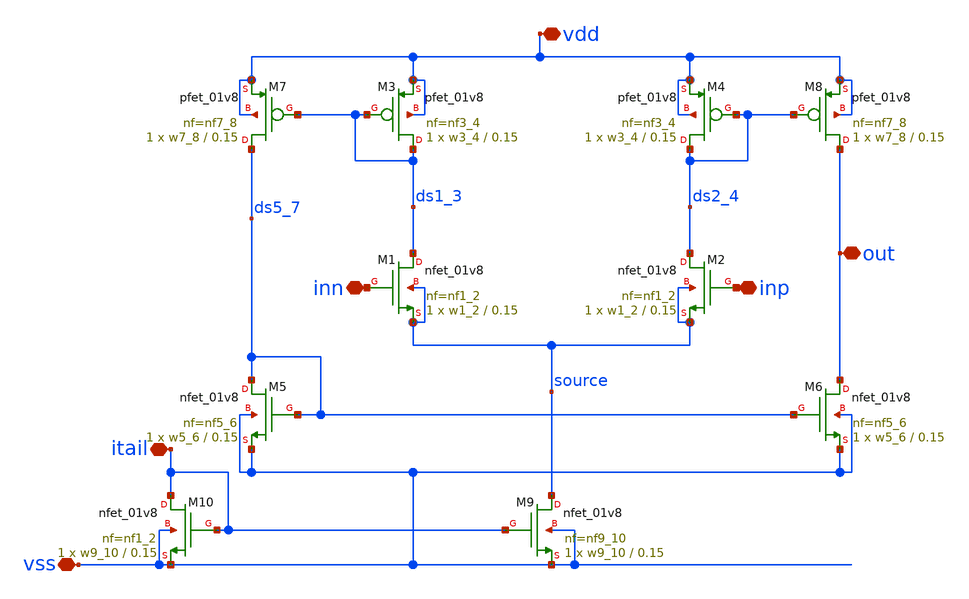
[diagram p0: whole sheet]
** sch_path: ISSCC25/submitted_notebooks/current_mirror_ota_optimization/characterization/sky130/schematics/cm_ota.sch
**.subckt cm_ota inn inp out vss vdd itail
*.iopin inn
*.iopin inp
*.iopin out
*.iopin vss
*.iopin vdd
*.iopin itail
XM1 ds1_3 inn source source sky130_fd_pr__nfet_01v8 L=0.15 W=w1_2 nf=nf1_2 ad='int((nf+1)/2) * W/nf * 0.29'
+ as='int((nf+2)/2) * W/nf * 0.29' pd='2*int((nf+1)/2) * (W/nf + 0.29)' ps='2*int((nf+2)/2) * (W/nf + 0.29)'
+ nrd='0.29 / W' nrs='0.29 / W' sa=0 sb=0 sd=0 mult=1 m=1
xM3 ds1_3 ds1_3 vdd vdd sky130_fd_pr__pfet_01v8 L=0.15 W=w3_4 nf=nf3_4 ad='int((nf+1)/2) * W/nf * 0.29'
+ as='int((nf+2)/2) * W/nf * 0.29' pd='2*int((nf+1)/2) * (W/nf + 0.29)' ps='2*int((nf+2)/2) * (W/nf + 0.29)'
+ nrd='0.29 / W' nrs='0.29 / W' sa=0 sb=0 sd=0 mult=1 m=1
XM2 ds2_4 inp source source sky130_fd_pr__nfet_01v8 L=0.15 W=w1_2 nf=nf1_2 ad='int((nf+1)/2) * W/nf * 0.29'
+ as='int((nf+2)/2) * W/nf * 0.29' pd='2*int((nf+1)/2) * (W/nf + 0.29)' ps='2*int((nf+2)/2) * (W/nf + 0.29)'
+ nrd='0.29 / W' nrs='0.29 / W' sa=0 sb=0 sd=0 mult=1 m=1
xM4 ds2_4 ds2_4 vdd vdd sky130_fd_pr__pfet_01v8 L=0.15 W=w3_4 nf=nf3_4 ad='int((nf+1)/2) * W/nf * 0.29'
+ as='int((nf+2)/2) * W/nf * 0.29' pd='2*int((nf+1)/2) * (W/nf + 0.29)' ps='2*int((nf+2)/2) * (W/nf + 0.29)'
+ nrd='0.29 / W' nrs='0.29 / W' sa=0 sb=0 sd=0 mult=1 m=1
xM7 ds5_7 ds1_3 vdd vdd sky130_fd_pr__pfet_01v8 L=0.15 W=w7_8 nf=nf7_8 ad='int((nf+1)/2) * W/nf * 0.29'
+ as='int((nf+2)/2) * W/nf * 0.29' pd='2*int((nf+1)/2) * (W/nf + 0.29)' ps='2*int((nf+2)/2) * (W/nf + 0.29)'
+ nrd='0.29 / W' nrs='0.29 / W' sa=0 sb=0 sd=0 mult=1 m=1
XM5 ds5_7 ds5_7 vss vss sky130_fd_pr__nfet_01v8 L=0.15 W=w5_6 nf=nf5_6 ad='int((nf+1)/2) * W/nf * 0.29'
+ as='int((nf+2)/2) * W/nf * 0.29' pd='2*int((nf+1)/2) * (W/nf + 0.29)' ps='2*int((nf+2)/2) * (W/nf + 0.29)'
+ nrd='0.29 / W' nrs='0.29 / W' sa=0 sb=0 sd=0 mult=1 m=1
XM6 out ds5_7 vss vss sky130_fd_pr__nfet_01v8 L=0.15 W=w5_6 nf=nf5_6 ad='int((nf+1)/2) * W/nf * 0.29'
+ as='int((nf+2)/2) * W/nf * 0.29' pd='2*int((nf+1)/2) * (W/nf + 0.29)' ps='2*int((nf+2)/2) * (W/nf + 0.29)'
+ nrd='0.29 / W' nrs='0.29 / W' sa=0 sb=0 sd=0 mult=1 m=1
xM8 out ds2_4 vdd vdd sky130_fd_pr__pfet_01v8 L=0.15 W=w7_8 nf=nf7_8 ad='int((nf+1)/2) * W/nf * 0.29'
+ as='int((nf+2)/2) * W/nf * 0.29' pd='2*int((nf+1)/2) * (W/nf + 0.29)' ps='2*int((nf+2)/2) * (W/nf + 0.29)'
+ nrd='0.29 / W' nrs='0.29 / W' sa=0 sb=0 sd=0 mult=1 m=1
XM9 source itail vss vss sky130_fd_pr__nfet_01v8 L=0.15 W=w9_10 nf=nf9_10 ad='int((nf+1)/2) * W/nf * 0.29'
+ as='int((nf+2)/2) * W/nf * 0.29' pd='2*int((nf+1)/2) * (W/nf + 0.29)' ps='2*int((nf+2)/2) * (W/nf + 0.29)'
+ nrd='0.29 / W' nrs='0.29 / W' sa=0 sb=0 sd=0 mult=1 m=1
XM10 itail itail vss vss sky130_fd_pr__nfet_01v8 L=0.15 W=w9_10 nf=nf1_2 ad='int((nf+1)/2) * W/nf * 0.29'
+ as='int((nf+2)/2) * W/nf * 0.29' pd='2*int((nf+1)/2) * (W/nf + 0.29)' ps='2*int((nf+2)/2) * (W/nf + 0.29)'
+ nrd='0.29 / W' nrs='0.29 / W' sa=0 sb=0 sd=0 mult=1 m=1
**.ends
.end
